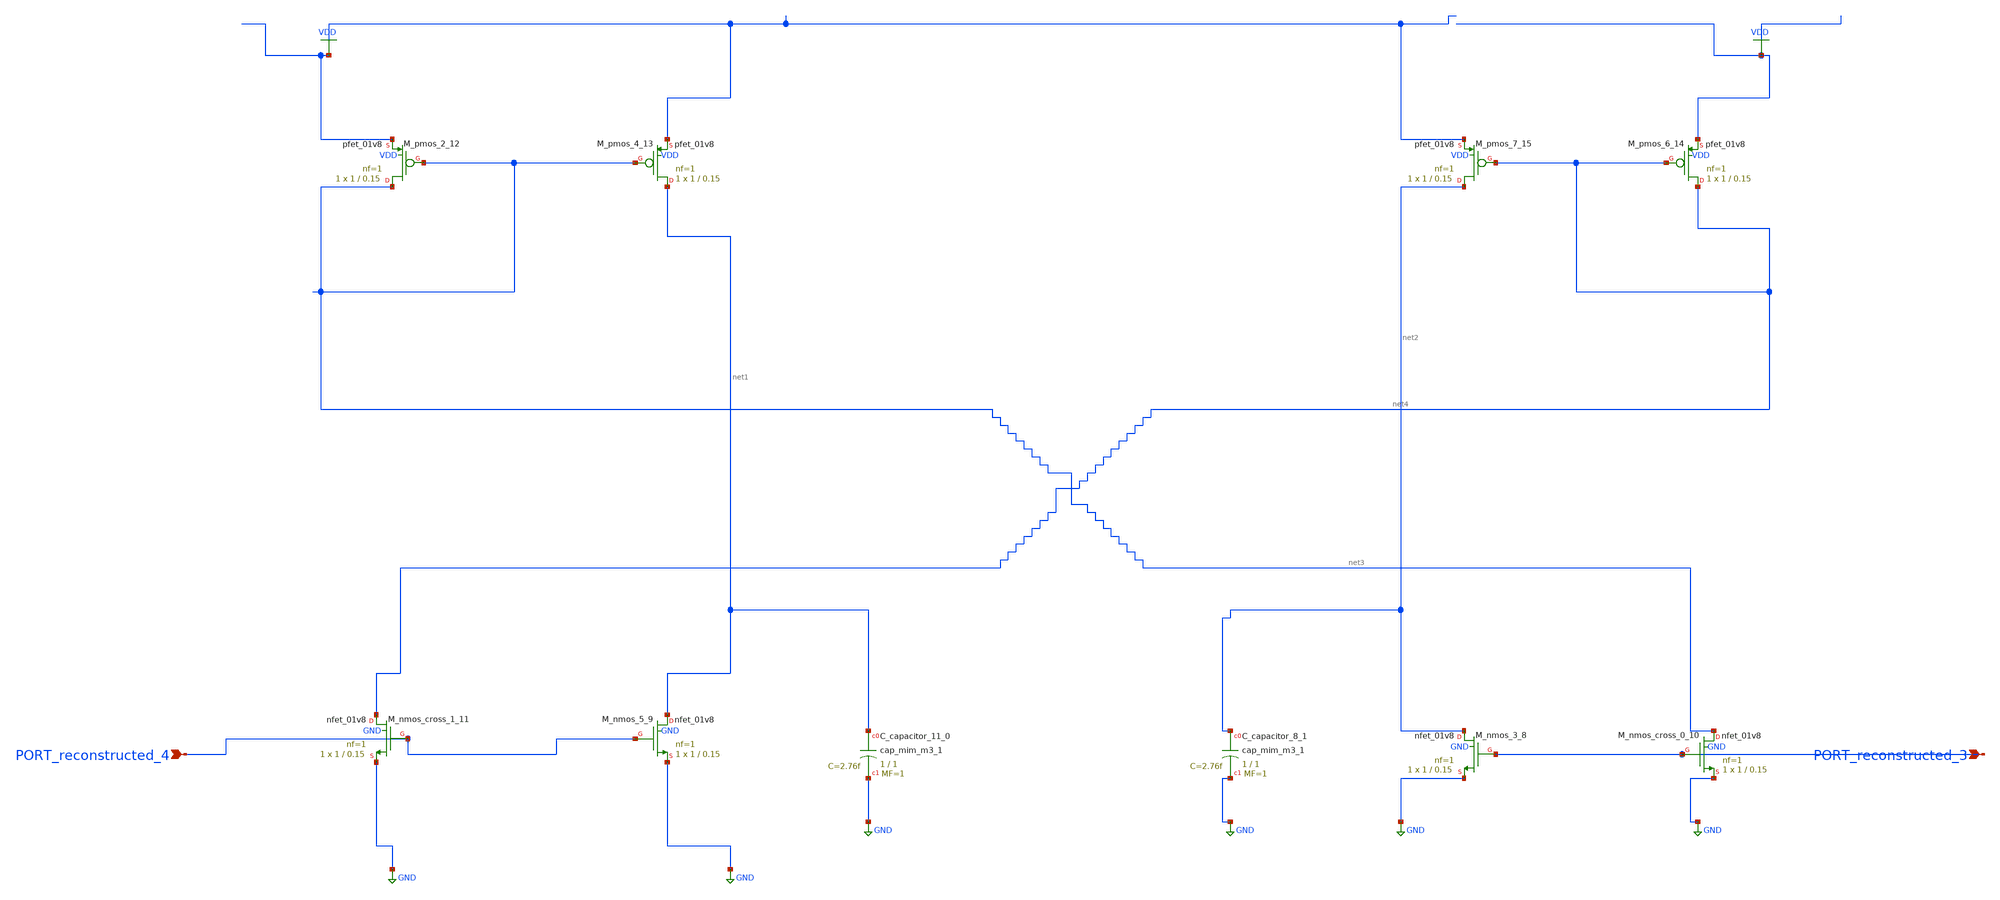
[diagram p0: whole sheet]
** sch_path: schematics/AMSNet/703.sch
**.subckt 703 PORT_reconstructed_3 PORT_reconstructed_4
*.ipin PORT_reconstructed_3
*.ipin PORT_reconstructed_4
XC_capacitor_11_0 net1 GND sky130_fd_pr__cap_mim_m3_1 W=1 L=1 MF=1 m=1
XC_capacitor_8_1 net2 GND sky130_fd_pr__cap_mim_m3_1 W=1 L=1 MF=1 m=1
XM_nmos_3_8 net2 PORT_reconstructed_3 GND GND sky130_fd_pr__nfet_01v8 L=0.15 W=1 nf=1 ad='int((1 + 1)/2) * 1 / 1 * 0.29'
+ as='int((1 + 2)/2) * 1 / 1 * 0.29' pd='2*int((1 + 1)/2) * (1 / 1 + 0.29)' ps='2*int((1 + 2)/2) * (1 / 1 + 0.29)'
+ nrd='0.29 / 1 ' nrs='0.29 / 1 ' sa=0 sb=0 sd=0 mult=1 m=1
XM_nmos_5_9 net1 PORT_reconstructed_4 GND GND sky130_fd_pr__nfet_01v8 L=0.15 W=1 nf=1 ad='int((1 + 1)/2) * 1 / 1 * 0.29'
+ as='int((1 + 2)/2) * 1 / 1 * 0.29' pd='2*int((1 + 1)/2) * (1 / 1 + 0.29)' ps='2*int((1 + 2)/2) * (1 / 1 + 0.29)'
+ nrd='0.29 / 1 ' nrs='0.29 / 1 ' sa=0 sb=0 sd=0 mult=1 m=1
XM_nmos_cross_0_10 net3 PORT_reconstructed_3 GND GND sky130_fd_pr__nfet_01v8 L=0.15 W=1 nf=1 ad='int((1 + 1)/2) * 1 / 1 * 0.29'
+ as='int((1 + 2)/2) * 1 / 1 * 0.29' pd='2*int((1 + 1)/2) * (1 / 1 + 0.29)' ps='2*int((1 + 2)/2) * (1 / 1 + 0.29)'
+ nrd='0.29 / 1 ' nrs='0.29 / 1 ' sa=0 sb=0 sd=0 mult=1 m=1
XM_nmos_cross_1_11 net4 PORT_reconstructed_4 GND GND sky130_fd_pr__nfet_01v8 L=0.15 W=1 nf=1 ad='int((1 + 1)/2) * 1 / 1 * 0.29'
+ as='int((1 + 2)/2) * 1 / 1 * 0.29' pd='2*int((1 + 1)/2) * (1 / 1 + 0.29)' ps='2*int((1 + 2)/2) * (1 / 1 + 0.29)'
+ nrd='0.29 / 1 ' nrs='0.29 / 1 ' sa=0 sb=0 sd=0 mult=1 m=1
XM_pmos_2_12 net3 net3 VDD VDD sky130_fd_pr__pfet_01v8 L=0.15 W=1 nf=1 ad='int((1 + 1)/2) * 1 / 1 * 0.29'
+ as='int((1 + 2)/2) * 1 / 1 * 0.29' pd='2*int((1 + 1)/2) * (1 / 1 + 0.29)' ps='2*int((1 + 2)/2) * (1 / 1 + 0.29)'
+ nrd='0.29 / 1 ' nrs='0.29 / 1 ' sa=0 sb=0 sd=0 mult=1 m=1
XM_pmos_4_13 net1 net3 VDD VDD sky130_fd_pr__pfet_01v8 L=0.15 W=1 nf=1 ad='int((1 + 1)/2) * 1 / 1 * 0.29'
+ as='int((1 + 2)/2) * 1 / 1 * 0.29' pd='2*int((1 + 1)/2) * (1 / 1 + 0.29)' ps='2*int((1 + 2)/2) * (1 / 1 + 0.29)'
+ nrd='0.29 / 1 ' nrs='0.29 / 1 ' sa=0 sb=0 sd=0 mult=1 m=1
XM_pmos_6_14 net4 net4 VDD VDD sky130_fd_pr__pfet_01v8 L=0.15 W=1 nf=1 ad='int((1 + 1)/2) * 1 / 1 * 0.29'
+ as='int((1 + 2)/2) * 1 / 1 * 0.29' pd='2*int((1 + 1)/2) * (1 / 1 + 0.29)' ps='2*int((1 + 2)/2) * (1 / 1 + 0.29)'
+ nrd='0.29 / 1 ' nrs='0.29 / 1 ' sa=0 sb=0 sd=0 mult=1 m=1
XM_pmos_7_15 net2 net4 VDD VDD sky130_fd_pr__pfet_01v8 L=0.15 W=1 nf=1 ad='int((1 + 1)/2) * 1 / 1 * 0.29'
+ as='int((1 + 2)/2) * 1 / 1 * 0.29' pd='2*int((1 + 1)/2) * (1 / 1 + 0.29)' ps='2*int((1 + 2)/2) * (1 / 1 + 0.29)'
+ nrd='0.29 / 1 ' nrs='0.29 / 1 ' sa=0 sb=0 sd=0 mult=1 m=1
**.ends
.GLOBAL GND
.GLOBAL VDD
.end
